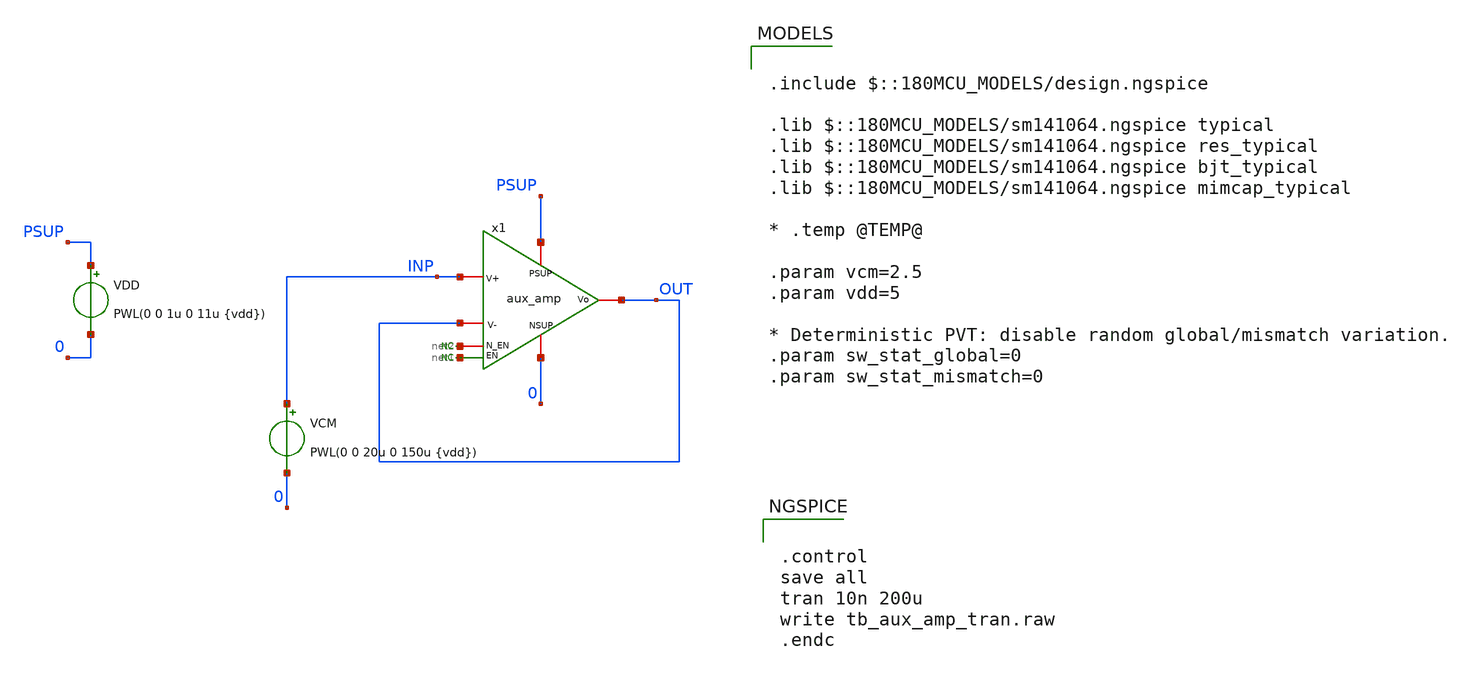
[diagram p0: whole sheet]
** sch_path: xschem/blocks/aux_amp/tb_aux_amp_tran.sch
**.subckt tb_aux_amp_tran
VDD PSUP 0 PWL(0 0 1u 0 11u {vdd})
VCM INP 0 PWL(0 0 20u 0 150u {vdd})
* noconn #net1
* noconn #net2
x1 PSUP OUT INP OUT net2 0 net1 aux_amp
**** begin user architecture code


.control
save all
tran 10n 200u
write tb_aux_amp_tran.raw
.endc



.include $::180MCU_MODELS/design.ngspice

.lib $::180MCU_MODELS/sm141064.ngspice typical
.lib $::180MCU_MODELS/sm141064.ngspice res_typical
.lib $::180MCU_MODELS/sm141064.ngspice bjt_typical
.lib $::180MCU_MODELS/sm141064.ngspice mimcap_typical

* .temp @TEMP@

.param vcm=2.5
.param vdd=5

* Deterministic PVT: disable random global/mismatch variation.
.param sw_stat_global=0
.param sw_stat_mismatch=0


**** end user architecture code
**.ends

* expanding   symbol:  blocks/aux_amp/aux_amp.sym # of pins=7
** sym_path: xschem/lib/aux_amp.sym
** sch_path: xschem/lib/aux_amp.sch
.subckt aux_amp PSUP Vo V+ V- N_EN NSUP EN
*.ipin PSUP
*.ipin NSUP
*.ipin N_EN
*.ipin EN
*.ipin V+
*.ipin V-
*.opin Vo
XM1 Vo V- net2 net2 nfet_06v0 L=1.80u W=0.80u nf=1 ad='int((nf+1)/2) * W/nf * 0.18u' as='int((nf+2)/2) * W/nf * 0.18u'
+ pd='2*int((nf+1)/2) * (W/nf + 0.18u)' ps='2*int((nf+2)/2) * (W/nf + 0.18u)' nrd='0.18u / W' nrs='0.18u / W'
+ sa=0 sb=0 sd=0 m=1
XM2 net1 V+ net2 net2 nfet_06v0 L=1.80u W=0.80u nf=1 ad='int((nf+1)/2) * W/nf * 0.18u' as='int((nf+2)/2) * W/nf * 0.18u'
+ pd='2*int((nf+1)/2) * (W/nf + 0.18u)' ps='2*int((nf+2)/2) * (W/nf + 0.18u)' nrd='0.18u / W' nrs='0.18u / W'
+ sa=0 sb=0 sd=0 m=1
XM5 net1 net1 PSUP PSUP pfet_06v0 L=0.55u W=0.30u nf=1 ad='int((nf+1)/2) * W/nf * 0.18u' as='int((nf+2)/2) * W/nf * 0.18u'
+ pd='2*int((nf+1)/2) * (W/nf + 0.18u)' ps='2*int((nf+2)/2) * (W/nf + 0.18u)' nrd='0.18u / W' nrs='0.18u / W'
+ sa=0 sb=0 sd=0 m=1
XM6 Vo net1 PSUP PSUP pfet_06v0 L=0.55u W=0.30u nf=1 ad='int((nf+1)/2) * W/nf * 0.18u' as='int((nf+2)/2) * W/nf * 0.18u'
+ pd='2*int((nf+1)/2) * (W/nf + 0.18u)' ps='2*int((nf+2)/2) * (W/nf + 0.18u)' nrd='0.18u / W' nrs='0.18u / W'
+ sa=0 sb=0 sd=0 m=1
I0 net2 NSUP 5u
* noconn N_EN
* noconn EN
.ends

.end
